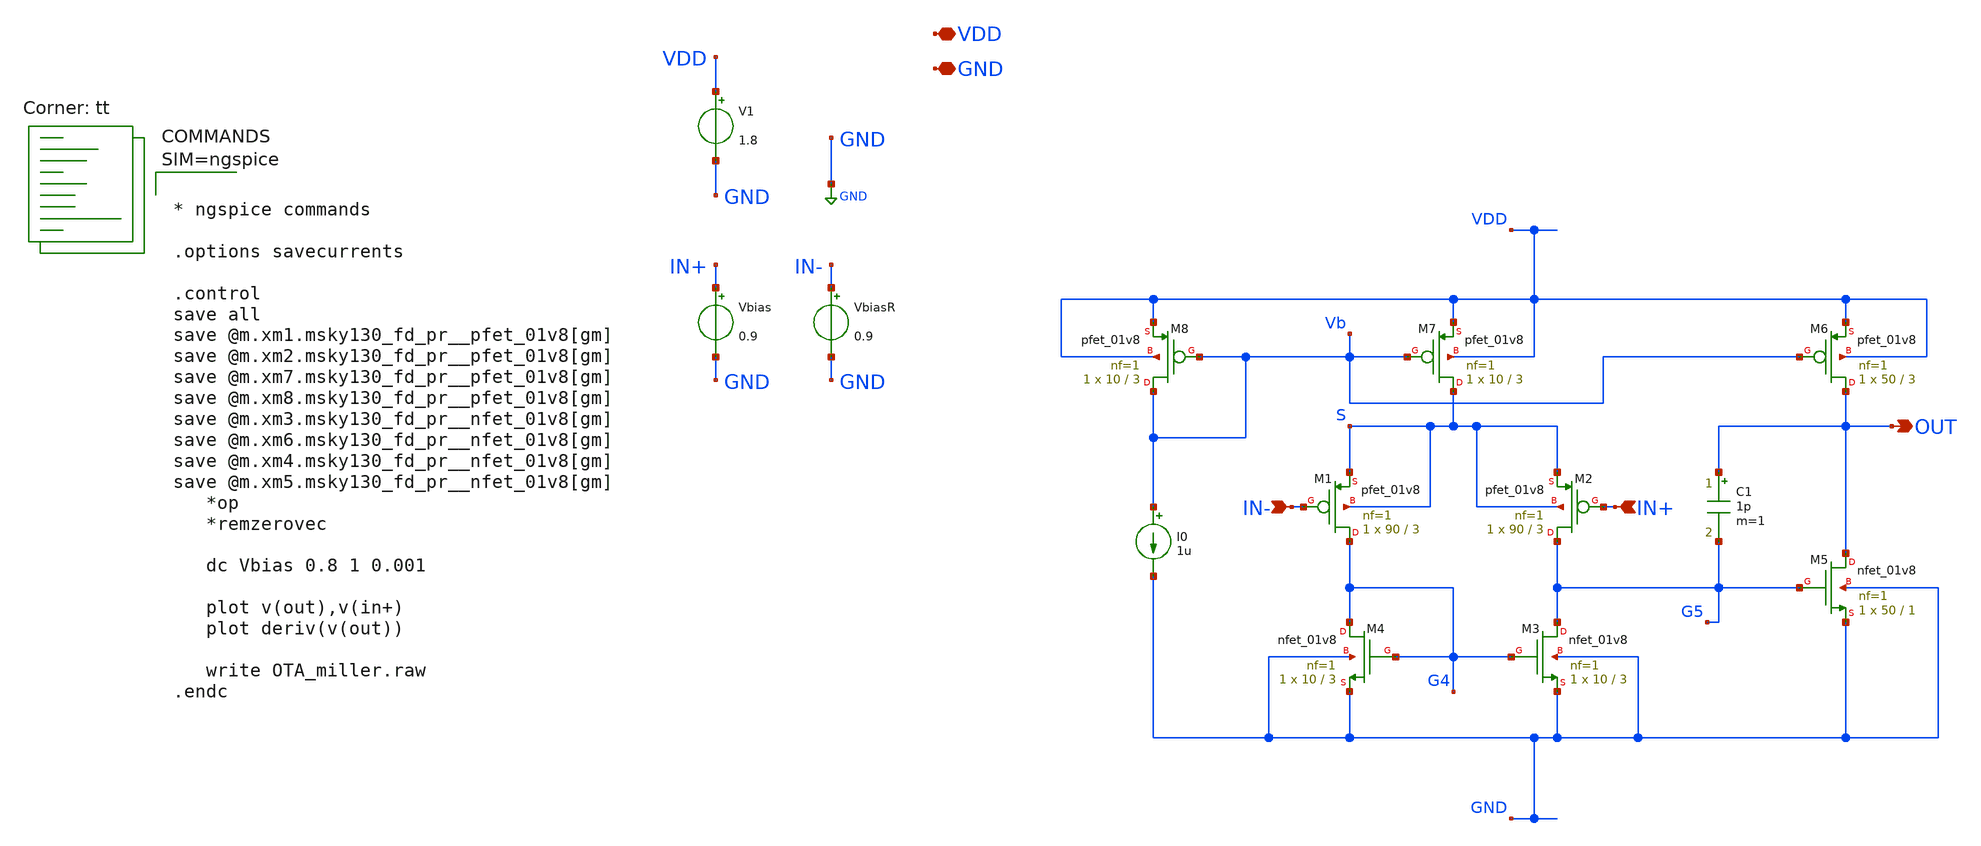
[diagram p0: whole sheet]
** sch_path: xschem/OTA_miller.sch
**.subckt OTA_miller VDD GND IN+ IN- OUT
*.iopin VDD
*.iopin GND
*.ipin IN+
*.ipin IN-
*.opin OUT
XM1 G4 IN- S S sky130_fd_pr__pfet_01v8 L=3 W=90 nf=1 ad='int((nf+1)/2) * W/nf * 0.29' as='int((nf+2)/2) * W/nf * 0.29'
+ pd='2*int((nf+1)/2) * (W/nf + 0.29)' ps='2*int((nf+2)/2) * (W/nf + 0.29)' nrd='0.29 / W' nrs='0.29 / W'
+ sa=0 sb=0 sd=0 mult=1 m=1
XM2 G5 IN+ S S sky130_fd_pr__pfet_01v8 L=3 W=90 nf=1 ad='int((nf+1)/2) * W/nf * 0.29' as='int((nf+2)/2) * W/nf * 0.29'
+ pd='2*int((nf+1)/2) * (W/nf + 0.29)' ps='2*int((nf+2)/2) * (W/nf + 0.29)' nrd='0.29 / W' nrs='0.29 / W'
+ sa=0 sb=0 sd=0 mult=1 m=1
XM3 G5 G4 GND GND sky130_fd_pr__nfet_01v8 L=3 W=10 nf=1 ad='int((nf+1)/2) * W/nf * 0.29' as='int((nf+2)/2) * W/nf * 0.29'
+ pd='2*int((nf+1)/2) * (W/nf + 0.29)' ps='2*int((nf+2)/2) * (W/nf + 0.29)' nrd='0.29 / W' nrs='0.29 / W'
+ sa=0 sb=0 sd=0 mult=1 m=1
XM4 G4 G4 GND GND sky130_fd_pr__nfet_01v8 L=3 W=10 nf=1 ad='int((nf+1)/2) * W/nf * 0.29' as='int((nf+2)/2) * W/nf * 0.29'
+ pd='2*int((nf+1)/2) * (W/nf + 0.29)' ps='2*int((nf+2)/2) * (W/nf + 0.29)' nrd='0.29 / W' nrs='0.29 / W'
+ sa=0 sb=0 sd=0 mult=1 m=1
XM5 OUT G5 GND GND sky130_fd_pr__nfet_01v8 L=1 W=50 nf=1 ad='int((nf+1)/2) * W/nf * 0.29' as='int((nf+2)/2) * W/nf * 0.29'
+ pd='2*int((nf+1)/2) * (W/nf + 0.29)' ps='2*int((nf+2)/2) * (W/nf + 0.29)' nrd='0.29 / W' nrs='0.29 / W'
+ sa=0 sb=0 sd=0 mult=1 m=1
XM6 OUT Vb VDD VDD sky130_fd_pr__pfet_01v8 L=3 W=50 nf=1 ad='int((nf+1)/2) * W/nf * 0.29' as='int((nf+2)/2) * W/nf * 0.29'
+ pd='2*int((nf+1)/2) * (W/nf + 0.29)' ps='2*int((nf+2)/2) * (W/nf + 0.29)' nrd='0.29 / W' nrs='0.29 / W'
+ sa=0 sb=0 sd=0 mult=1 m=1
XM7 S Vb VDD VDD sky130_fd_pr__pfet_01v8 L=3 W=10 nf=1 ad='int((nf+1)/2) * W/nf * 0.29' as='int((nf+2)/2) * W/nf * 0.29'
+ pd='2*int((nf+1)/2) * (W/nf + 0.29)' ps='2*int((nf+2)/2) * (W/nf + 0.29)' nrd='0.29 / W' nrs='0.29 / W'
+ sa=0 sb=0 sd=0 mult=1 m=1
XM8 Vb Vb VDD VDD sky130_fd_pr__pfet_01v8 L=3 W=10 nf=1 ad='int((nf+1)/2) * W/nf * 0.29' as='int((nf+2)/2) * W/nf * 0.29'
+ pd='2*int((nf+1)/2) * (W/nf + 0.29)' ps='2*int((nf+2)/2) * (W/nf + 0.29)' nrd='0.29 / W' nrs='0.29 / W'
+ sa=0 sb=0 sd=0 mult=1 m=1
I0 Vb GND 1u
V1 VDD GND 1.8
Vbias IN+ GND 0.9
VbiasR IN- GND 0.9
C1 OUT G5 1p m=1
**** begin user architecture code



* ngspice commands

.options savecurrents

.control
save all
save @m.xm1.msky130_fd_pr__pfet_01v8[gm]
save @m.xm2.msky130_fd_pr__pfet_01v8[gm]
save @m.xm7.msky130_fd_pr__pfet_01v8[gm]
save @m.xm8.msky130_fd_pr__pfet_01v8[gm]
save @m.xm3.msky130_fd_pr__nfet_01v8[gm]
save @m.xm6.msky130_fd_pr__nfet_01v8[gm]
save @m.xm4.msky130_fd_pr__nfet_01v8[gm]
save @m.xm5.msky130_fd_pr__nfet_01v8[gm]
   *op
   *remzerovec

   dc Vbias 0.8 1 0.001

   plot v(out),v(in+)
   plot deriv(v(out))

   write OTA_miller.raw
.endc




.lib $::SKYWATER_MODELS/sky130.lib.spice tt
**** end user architecture code
**.ends
.GLOBAL GND
.end
